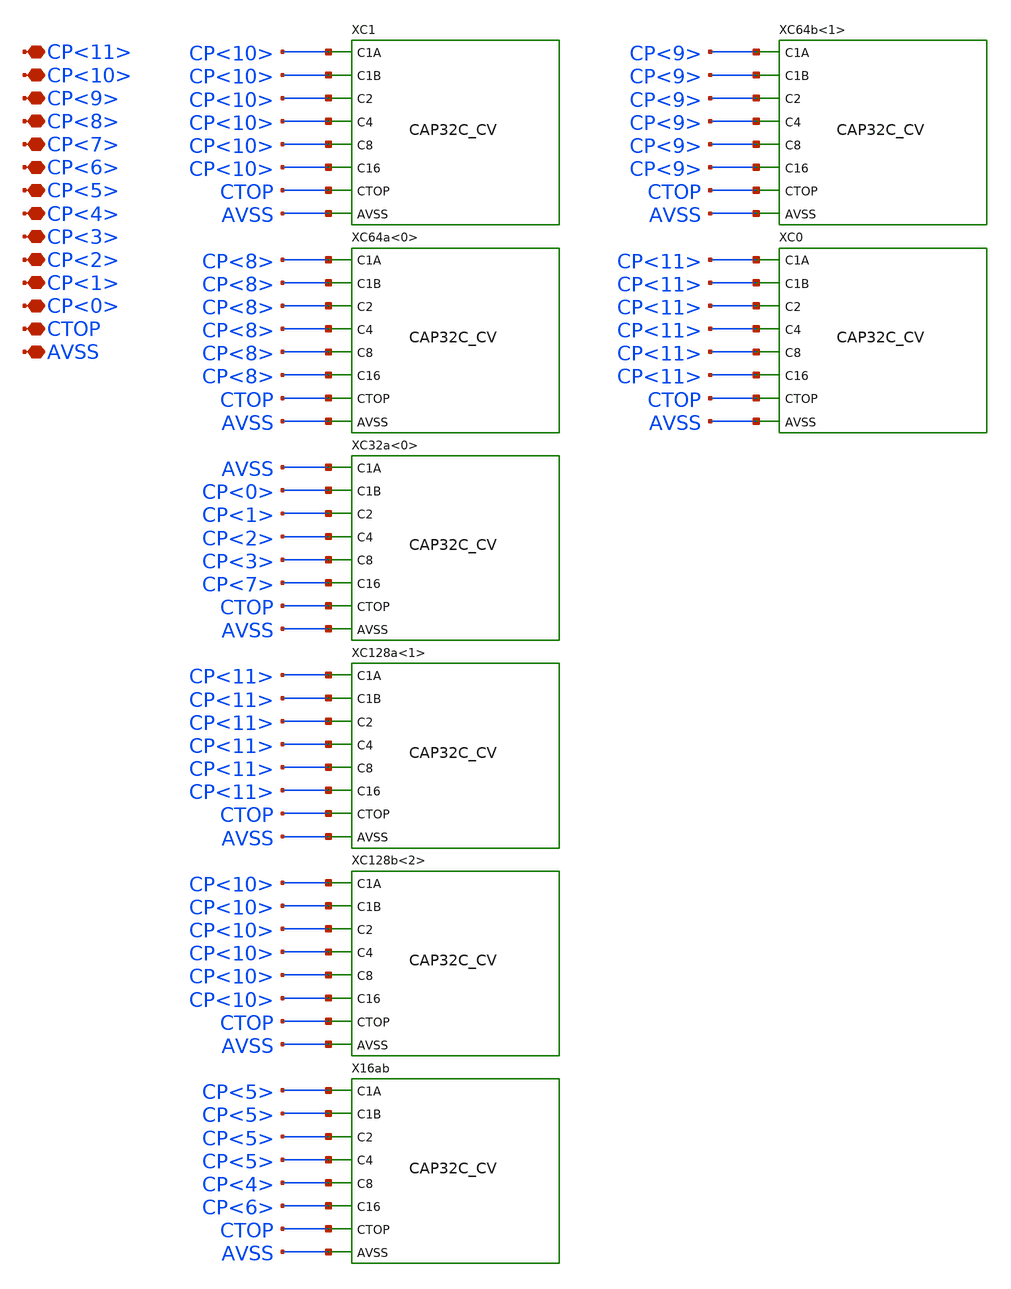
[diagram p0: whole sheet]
** sch_path: ip/sun_sar9b_sky130nm/design/SUN_SAR9B_SK130NM/CDAC8_CV.sch
**.subckt CDAC8_CV CP<11> CP<10> CP<9> CP<8> CP<7> CP<6> CP<5> CP<4> CP<3> CP<2> CP<1> CP<0> CTOP
*+ AVSS
*.iopin CP<11>
*.iopin CP<10>
*.iopin CP<9>
*.iopin CP<8>
*.iopin CP<7>
*.iopin CP<6>
*.iopin CP<5>
*.iopin CP<4>
*.iopin CP<3>
*.iopin CP<2>
*.iopin CP<1>
*.iopin CP<0>
*.iopin CTOP
*.iopin AVSS
XC1 CP<10> CP<10> CP<10> CP<10> CP<10> CP<10> CTOP AVSS CAP32C_CV
XC64a<0> CP<8> CP<8> CP<8> CP<8> CP<8> CP<8> CTOP AVSS CAP32C_CV
XC32a<0> AVSS CP<0> CP<1> CP<2> CP<3> CP<7> CTOP AVSS CAP32C_CV
XC128a<1> CP<11> CP<11> CP<11> CP<11> CP<11> CP<11> CTOP AVSS CAP32C_CV
XC128b<2> CP<10> CP<10> CP<10> CP<10> CP<10> CP<10> CTOP AVSS CAP32C_CV
X16ab CP<5> CP<5> CP<5> CP<5> CP<4> CP<6> CTOP AVSS CAP32C_CV
XC64b<1> CP<9> CP<9> CP<9> CP<9> CP<9> CP<9> CTOP AVSS CAP32C_CV
XC0 CP<11> CP<11> CP<11> CP<11> CP<11> CP<11> CTOP AVSS CAP32C_CV
**.ends
.end
